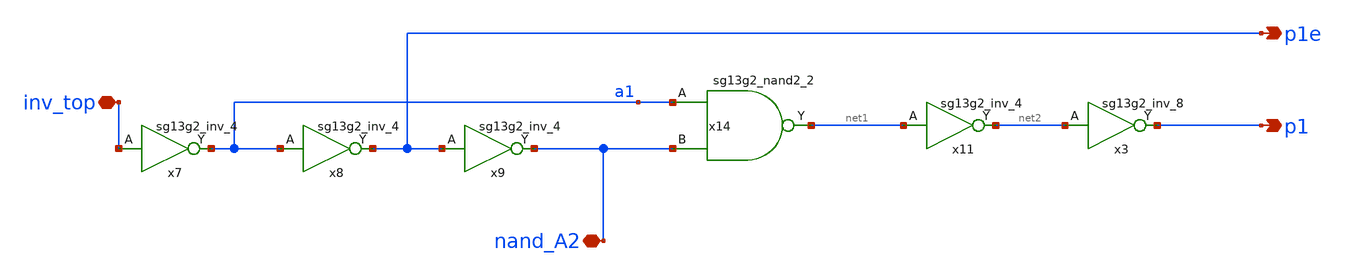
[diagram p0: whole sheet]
** sch_path: 5_Design/4_Layout/Team 5/xschem/clock_5_split1.sch
* IHP-GmbH/IHP-Open-PDK/ihp-sg13g2/libs.tech/xschem/sg13g2_stdcells/sg13g2_inv_4.sch:
* Copyright 2023 IHP PDK Authors
* Licensed under the Apache License, Version 2.0 (the "License");
**.subckt clock_5_split1 p1e p1 inv_top nand_A2
*.opin p1e
*.opin p1
*.iopin inv_top
*.iopin nand_A2
x7 a1 inv_top VDD VSS sg13g2_inv_4
x8 p1e a1 VDD VSS sg13g2_inv_4
x9 nand_A2 p1e VDD VSS sg13g2_inv_4
x11 net2 net1 VDD VSS sg13g2_inv_4
x3 p1 net2 VDD VSS sg13g2_inv_8
x14 net1 a1 nand_A2 VDD VSS sg13g2_nand2_2
**.ends

* expanding   symbol:  sg13g2_stdcells/sg13g2_inv_4.sym # of pins=2
** sym_path: sg13g2_stdcells/sg13g2_inv_4.sym
** sch_path: sg13g2_stdcells/sg13g2_inv_4.sch
.subckt sg13g2_inv_4 Y A VDD VSS
*.ipin A
*.opin Y
*.iopin VDD
*.iopin VSS
XM1 Y A VSS VSS sg13_lv_nmos w=2.96u l=130.00n ng=4 m=1 mm_ok=1
XM2 Y A VDD VDD sg13_lv_pmos w=4.48u l=130.00n ng=4 m=1 mm_ok=1
.ends


* expanding   symbol:  sg13g2_stdcells/sg13g2_inv_8.sym # of pins=2
** sym_path: sg13g2_stdcells/sg13g2_inv_8.sym
** sch_path: sg13g2_stdcells/sg13g2_inv_8.sch
.subckt sg13g2_inv_8 Y A VDD VSS
*.opin Y
*.ipin A
*.iopin VDD
*.iopin VSS
XM1 Y A VSS VSS sg13_lv_nmos w=5.92u l=130.00n ng=8 m=1 mm_ok=1
XM2 Y A VDD VDD sg13_lv_pmos w=8.96u l=130.00n ng=8 m=1 mm_ok=1
.ends


* expanding   symbol:  sg13g2_stdcells/sg13g2_nand2_2.sym # of pins=3
** sym_path: sg13g2_stdcells/sg13g2_nand2_2.sym
** sch_path: sg13g2_stdcells/sg13g2_nand2_2.sch
.subckt sg13g2_nand2_2 Y A B VDD VSS
*.iopin VDD
*.iopin VSS
*.opin Y
*.ipin B
*.ipin A
XM1 Y A net1 VSS sg13_lv_nmos w=1.44u l=130.00n ng=2 m=1 mm_ok=1
XM2 net1 B VSS VSS sg13_lv_nmos w=1.44u l=130.00n ng=2 m=1 mm_ok=1
XM3 Y A VDD VDD sg13_lv_pmos w=2.24u l=130.00n ng=2 m=1 mm_ok=1
XM4 Y B VDD VDD sg13_lv_pmos w=2.24u l=130.00n ng=2 m=1 mm_ok=1
.ends

.end
